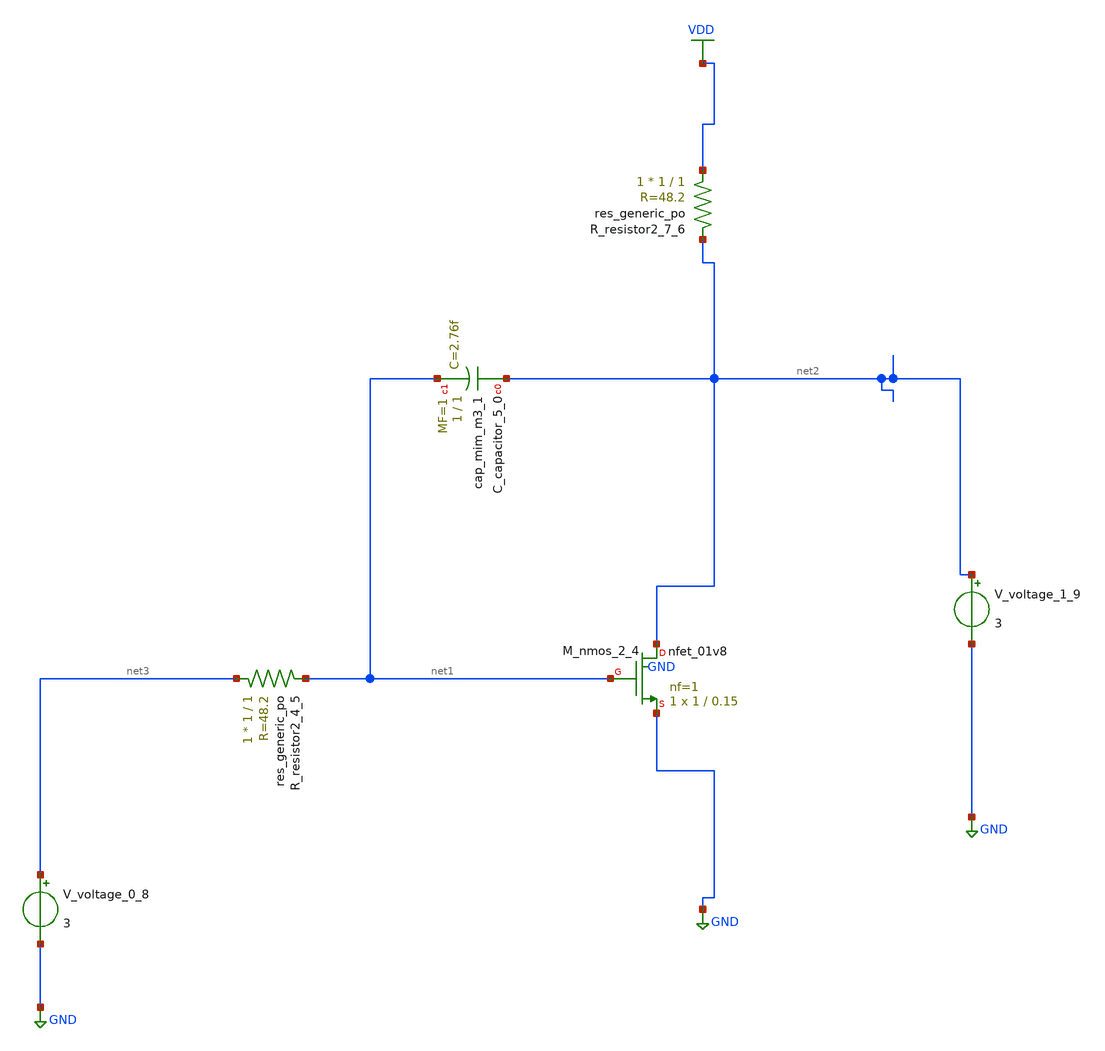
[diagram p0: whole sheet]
** sch_path: schematics/AMSNet/401.sch
**.subckt 401
XC_capacitor_5_0 net2 net1 sky130_fd_pr__cap_mim_m3_1 W=1 L=1 MF=1 m=1
XM_nmos_2_4 net2 net1 GND GND sky130_fd_pr__nfet_01v8 L=0.15 W=1 nf=1 ad='int((1 + 1)/2) * 1 / 1 * 0.29'
+ as='int((1 + 2)/2) * 1 / 1 * 0.29' pd='2*int((1 + 1)/2) * (1 / 1 + 0.29)' ps='2*int((1 + 2)/2) * (1 / 1 + 0.29)'
+ nrd='0.29 / 1 ' nrs='0.29 / 1 ' sa=0 sb=0 sd=0 mult=1 m=1
XR_resistor2_4_5 net3 net1 sky130_fd_pr__res_generic_po W=1 L=1 m=1
XR_resistor2_7_6 VDD net2 sky130_fd_pr__res_generic_po W=1 L=1 m=1
V_voltage_0_8 net3 GND 3
V_voltage_1_9 net2 GND 3
**.ends
.GLOBAL GND
.GLOBAL VDD
.end
